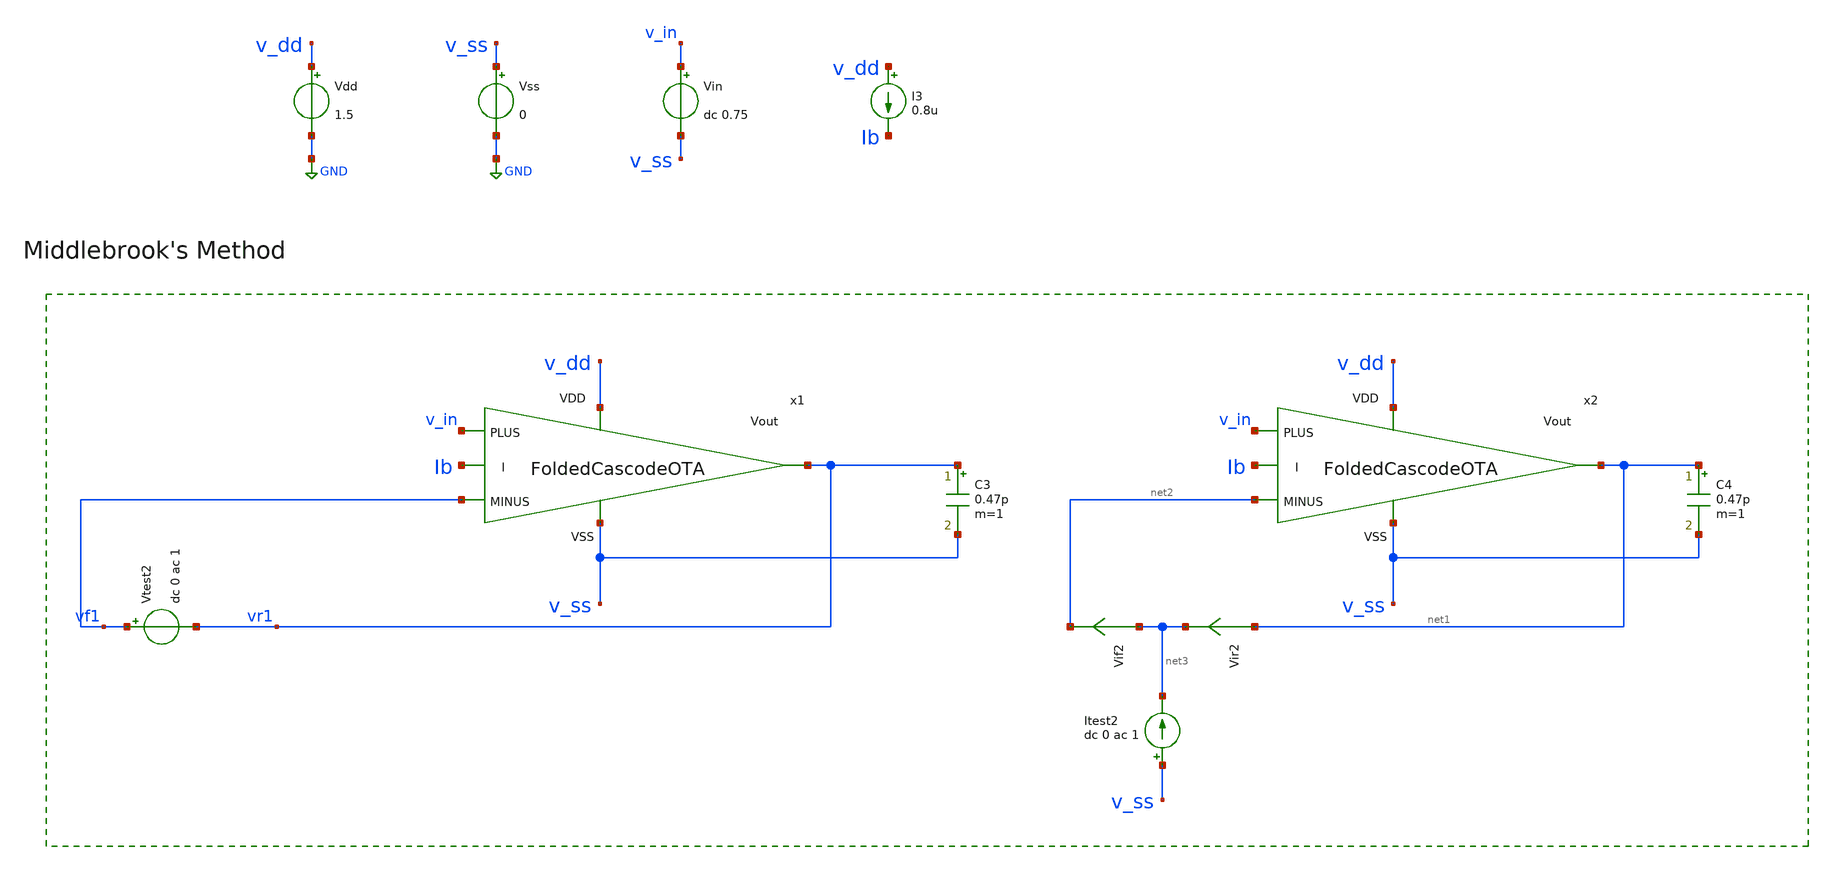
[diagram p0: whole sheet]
** sch_path: DSM/Schematics/Designs_Hrishi/RealCircuits/Folded Cascode/LoopGain.sch
* (c) 2024 Hrishikesh, @HSB
**.subckt LoopGain
C3 vr1 v_ss 0.47p m=1
I3 v_dd Ib 0.8u
Vtest2 vf1 vr1 dc 0 ac 1
C4 net1 v_ss 0.47p m=1
Itest2 v_ss net3 dc 0 ac 1
Vir2 net1 net3 0
.save i(vir2)
Vif2 net3 net2 0
.save i(vif2)
Vdd v_dd GND 1.5
Vss v_ss GND 0
Vin v_in v_ss dc 0.75
x1 v_dd Ib v_in vf1 vr1 v_ss FoldedCascodeOTA
x2 v_dd Ib v_in net2 net1 v_ss FoldedCascodeOTA
**** begin user architecture code
 .lib cornerMOSlv.lib mos_tt



.param temp=27
.options savecurrents reltol=1e-3 abstol=1e-12 gmin=1e-15
.control
save all

* Operating Point Analysis
op
remzerovec
write tb-loopgain.raw
set appendwrite

* AC Analysis
ac dec 101 1 100G
remzerovec
write tb-loopgain.raw
set appendwrite

* Middlebrook's Method
let tv=-v(vr1)/v(vf1)
let ti=-i(vir1)/i(vif1)
let tmb=(tv*ti - 1)/(tv + ti + 2)

plot db(tmb) ylabel 'Magnitude - Middlebrook'
plot 180/pi*cphase(tmb) ylabel 'Phase - Middlebrook'




*quit
.endc


**** end user architecture code
**.ends

* expanding   symbol:  /foss/designs/CEMS_DSM/DSM/Schematics/IC_Designs_Hrishi/RealCircuits/Folded Cascode/FoldedCascodeOTA.sym # of pins=6
** sym_path: DSM/Schematics/IC_Designs_Hrishi/RealCircuits/Folded Cascode/FoldedCascodeOTA.sym
** sch_path: DSM/Schematics/IC_Designs_Hrishi/RealCircuits/Folded Cascode/FoldedCascodeOTA.sch
.subckt FoldedCascodeOTA VDD I PLUS MINUS Vout VSS
*.ipin PLUS
*.ipin MINUS
*.opin Vout
*.ipin VDD
*.ipin VSS
*.ipin I
XM1 net2 net4 VDD VDD sg13_lv_pmos w=0.272u l=0.5u ng=1 m=1 mm_ok=1
XM2 net1 PLUS net2 VDD sg13_lv_pmos w=0.136u l=0.5u ng=1 m=1 mm_ok=1
XM3 net6 MINUS net2 VDD sg13_lv_pmos w=0.136u l=0.5u ng=1 m=1 mm_ok=1
XM14 net6 net9 VSS VSS sg13_lv_nmos w=0.30u l=2u ng=1 m=1 mm_ok=1
XM13 Vout I net6 VSS sg13_lv_nmos w=0.15u l=2u ng=1 m=1 mm_ok=1
XM11 net7 I net1 VSS sg13_lv_nmos w=0.15u l=2u ng=1 m=1 mm_ok=1
XM12 net1 net9 VSS VSS sg13_lv_nmos w=0.30u l=2u ng=1 m=1 mm_ok=1
XM5 Vout net3 net5 VDD sg13_lv_pmos w=0.136u l=0.5u ng=1 m=1 mm_ok=1
XM4 net5 net4 VDD VDD sg13_lv_pmos w=0.136u l=0.5u ng=1 m=1 mm_ok=1
XM6 net4 net4 VDD VDD sg13_lv_pmos w=0.136u l=0.5u ng=1 m=1 mm_ok=1
XM8 net3 net3 net4 VDD sg13_lv_pmos w=0.136u l=0.5u ng=1 m=1 mm_ok=1
XM9 net8 net4 VDD VDD sg13_lv_pmos w=0.136u l=0.5u ng=1 m=1 mm_ok=1
XM10 net7 net3 net8 VDD sg13_lv_pmos w=0.136u l=0.5u ng=1 m=1 mm_ok=1
XM16 I I net9 VSS sg13_lv_nmos w=0.15u l=2u ng=1 m=1 mm_ok=1
XM15 net9 net9 VSS VSS sg13_lv_nmos w=0.15u l=2u ng=1 m=1 mm_ok=1
XM7 net3 net9 VSS VSS sg13_lv_nmos w=0.15u l=2u ng=1 m=1 mm_ok=1
XM18 VDD I net10 VSS sg13_lv_nmos w=0.15u l=2u ng=1 m=1 mm_ok=1
XM17 net10 net9 VSS VSS sg13_lv_nmos w=0.15u l=2u ng=1 m=1 mm_ok=1
.ends

.GLOBAL GND
.end
